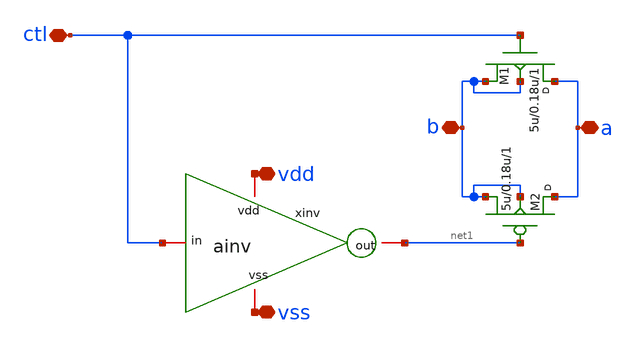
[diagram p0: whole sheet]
** sch_path: samples/digital_cosimulation/mos_tgate/symbol/mos_tgate.sch


.model p1 pmos   level=2 vto=-0.5 kp=8.5e-6 gamma=0.4 phi=0.65 lambda=0.05 xj=0.5e-6
.model n1 nmos   level=2 vto=0.5 kp=24e-6 gamma=0.15 phi=0.65 lambda=0.015 xj=0.5e-6


**.subckt mos_tgate vdd ctl vss b a
*.iopin vdd
*.iopin ctl
*.iopin vss
*.iopin b
*.iopin a
xinv ctl net1 vdd vss ainv
M1 a ctl b b n1 w=5u l=0.18u m=1
M2 a net1 b b p1 w=5u l=0.18u m=1
**.ends

* expanding   symbol:  symbol/ainv.sym # of pins=4
** sym_path: samples/digital_cosimulation/ainv/symbol/ainv.sym
** sch_path: samples/digital_cosimulation/ainv/symbol/ainv.sch
.subckt ainv in out vdd vss
*.iopin vdd
*.iopin out
*.iopin vss
*.iopin in
**** begin user architecture code


.model p1 pmos   level=2 vto=-0.5 kp=8.5e-6 gamma=0.4 phi=0.65 lambda=0.05 xj=0.5e-6
.model n1 nmos   level=2 vto=0.5 kp=24e-6 gamma=0.15 phi=0.65 lambda=0.015 xj=0.5e-6


**** end user architecture code
mn out in vss vss n1 w=5u l=0.18u m=1
mp out in vdd vdd p1 w=5u l=0.18u m=1
.ends

.end
